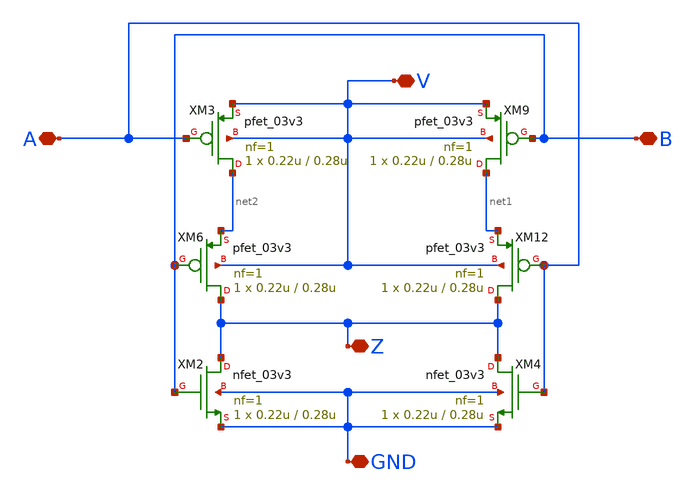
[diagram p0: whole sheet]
** sch_path: SAR_ADC/xschem/spice/norgate.sch
**.subckt norgate GND A B V Z
*.iopin GND
*.iopin A
*.iopin B
*.iopin V
*.iopin Z
XM3 net2 A V V pfet_03v3 L=0.28u W=0.22u nf=1 ad='int((nf+1)/2) * W/nf * 0.18u' as='int((nf+2)/2) * W/nf * 0.18u'
+ pd='2*int((nf+1)/2) * (W/nf + 0.18u)' ps='2*int((nf+2)/2) * (W/nf + 0.18u)' nrd='0.18u / W' nrs='0.18u / W'
+ sa=0 sb=0 sd=0 m=1
XM6 Z B net2 V pfet_03v3 L=0.28u W=0.22u nf=1 ad='int((nf+1)/2) * W/nf * 0.18u' as='int((nf+2)/2) * W/nf * 0.18u'
+ pd='2*int((nf+1)/2) * (W/nf + 0.18u)' ps='2*int((nf+2)/2) * (W/nf + 0.18u)' nrd='0.18u / W' nrs='0.18u / W'
+ sa=0 sb=0 sd=0 m=1
XM9 net1 B V V pfet_03v3 L=0.28u W=0.22u nf=1 ad='int((nf+1)/2) * W/nf * 0.18u' as='int((nf+2)/2) * W/nf * 0.18u'
+ pd='2*int((nf+1)/2) * (W/nf + 0.18u)' ps='2*int((nf+2)/2) * (W/nf + 0.18u)' nrd='0.18u / W' nrs='0.18u / W'
+ sa=0 sb=0 sd=0 m=1
XM12 Z A net1 V pfet_03v3 L=0.28u W=0.22u nf=1 ad='int((nf+1)/2) * W/nf * 0.18u' as='int((nf+2)/2) * W/nf * 0.18u'
+ pd='2*int((nf+1)/2) * (W/nf + 0.18u)' ps='2*int((nf+2)/2) * (W/nf + 0.18u)' nrd='0.18u / W' nrs='0.18u / W'
+ sa=0 sb=0 sd=0 m=1
XM2 Z B GND GND nfet_03v3 L=0.28u W=0.22u nf=1 ad='int((nf+1)/2) * W/nf * 0.18u' as='int((nf+2)/2) * W/nf * 0.18u'
+ pd='2*int((nf+1)/2) * (W/nf + 0.18u)' ps='2*int((nf+2)/2) * (W/nf + 0.18u)' nrd='0.18u / W' nrs='0.18u / W'
+ sa=0 sb=0 sd=0 m=1
XM4 Z A GND GND nfet_03v3 L=0.28u W=0.22u nf=1 ad='int((nf+1)/2) * W/nf * 0.18u' as='int((nf+2)/2) * W/nf * 0.18u'
+ pd='2*int((nf+1)/2) * (W/nf + 0.18u)' ps='2*int((nf+2)/2) * (W/nf + 0.18u)' nrd='0.18u / W' nrs='0.18u / W'
+ sa=0 sb=0 sd=0 m=1
**** begin user architecture code

.include /foss/pdks/gf180mcuC/libs.tech/ngspice/design.ngspice
.lib /foss/pdks/gf180mcuC/libs.tech/ngspice/sm141064.ngspice typical

**** end user architecture code
**.ends
.end
